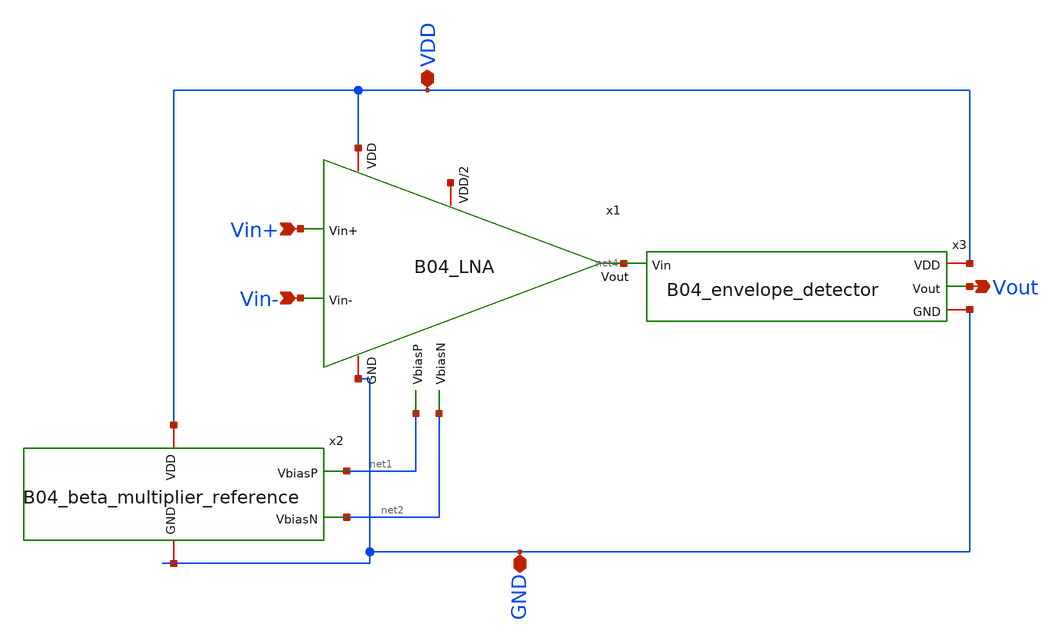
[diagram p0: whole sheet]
** sch_path: analog/B04_top_test.sch
**.subckt B04_top_test Vin+ Vin- Vout VDD GND
*.ipin Vin+
*.ipin Vin-
*.opin Vout
*.iopin VDD
*.iopin GND
x1 VDD net3 Vin+ net4 Vin- GND net1 net2 B04_LNA
x2 VDD net1 net2 GND B04_beta_multiplier_reference length=410u
x3 VDD net4 Vout GND B04_envelope_detector
**.ends
.end
